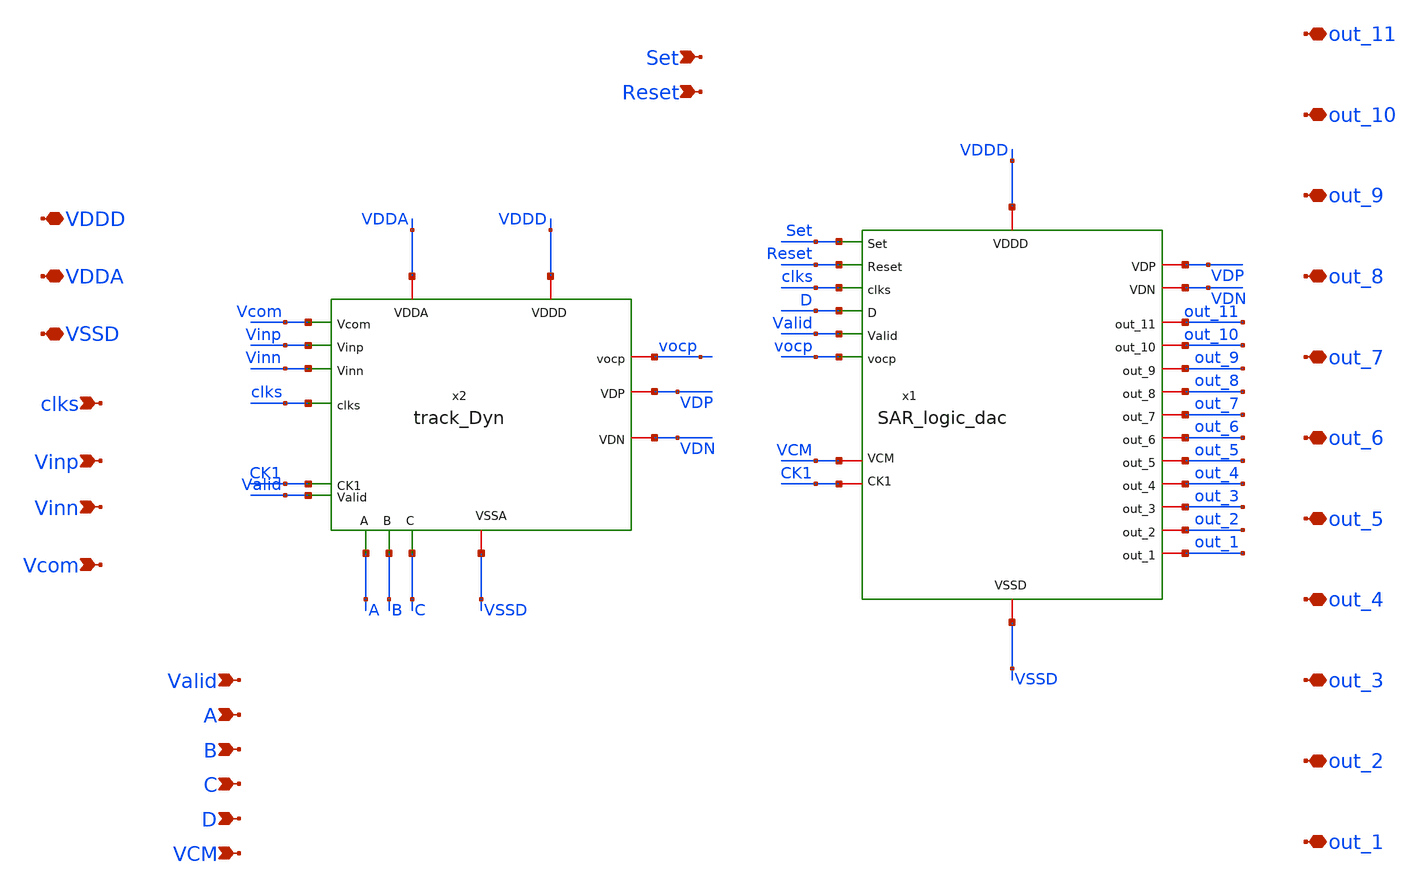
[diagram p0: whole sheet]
** sch_path: SAR_ADC/SAR_top/xschem/SAR_top.sch
**.subckt SAR_top VDDA VSSD clks Vinp Vinn Vcom VDDD Valid A B C out_11 out_10 out_9 out_8 out_7
*+ out_6 out_5 out_4 out_3 out_2 out_1 Set Reset D VCM
*.iopin VDDA
*.iopin VSSD
*.ipin clks
*.ipin Vinp
*.ipin Vinn
*.ipin Vcom
*.iopin VDDD
*.ipin Valid
*.ipin A
*.ipin B
*.ipin C
*.iopin out_11
*.iopin out_10
*.iopin out_9
*.iopin out_8
*.iopin out_7
*.iopin out_6
*.iopin out_5
*.iopin out_4
*.iopin out_3
*.iopin out_2
*.iopin out_1
*.ipin Set
*.ipin Reset
*.ipin D
*.ipin VCM
x1 VDP VDN out_11 out_10 VDDD out_9 VSSD VCM out_8 Set out_7 Reset clks out_6 D Valid out_5 vocp
+ out_4 out_3 out_2 out_1 CK1 SAR_logic_dac
x2 vocp VDDD VDP VDDA VDN VSSD clks Vinp Vinn CK1 Vcom Valid A B C track_Dyn
**.ends
.end
